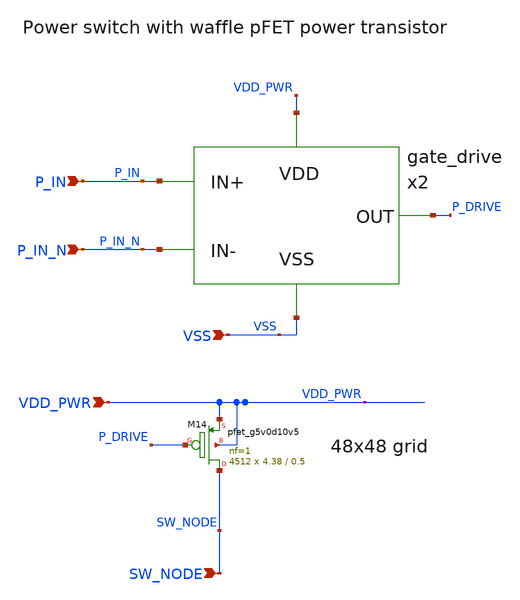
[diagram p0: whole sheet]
** sch_path: xschem/power_stage.sch
**.subckt power_stage P_IN P_IN_N SW_NODE VDD_PWR VSS
*.ipin P_IN
*.ipin P_IN_N
*.ipin SW_NODE
*.ipin VDD_PWR
*.ipin VSS
XM14 SW_NODE P_DRIVE VDD_PWR VDD_PWR sky130_fd_pr__pfet_g5v0d10v5 L=0.5 W=4.38 nf=1 ad='int((nf+1)/2) * W/nf * 0.29'
+ as='int((nf+2)/2) * W/nf * 0.29' pd='2*int((nf+1)/2) * (W/nf + 0.29)' ps='2*int((nf+2)/2) * (W/nf + 0.29)'
+ nrd='0.29 / W' nrs='0.29 / W' sa=0 sb=0 sd=0 mult=4512 m=4512
x2 P_IN P_IN_N VDD_PWR VSS P_DRIVE gate_drive
**.ends

* expanding   symbol:  gate_drive.sym # of pins=5
** sym_path: gate_drive.sym
** sch_path: gate_drive.sch
.subckt gate_drive IN_P IN_M VDD VSS OUT
*.ipin IN_M
*.ipin IN_P
*.ipin VDD
*.ipin VSS
*.opin OUT
XM1 net1 IN_P VSS VSS sky130_fd_pr__nfet_g5v0d10v5 L=0.5 W=2 nf=1 ad='int((nf+1)/2) * W/nf * 0.29' as='int((nf+2)/2) * W/nf * 0.29'
+ pd='2*int((nf+1)/2) * (W/nf + 0.29)' ps='2*int((nf+2)/2) * (W/nf + 0.29)' nrd='0.29 / W' nrs='0.29 / W'
+ sa=0 sb=0 sd=0 mult=2 m=2
XM2 net1 S1_N VDD VDD sky130_fd_pr__pfet_g5v0d10v5 L=0.5 W=4 nf=1 ad='int((nf+1)/2) * W/nf * 0.29' as='int((nf+2)/2) * W/nf * 0.29'
+ pd='2*int((nf+1)/2) * (W/nf + 0.29)' ps='2*int((nf+2)/2) * (W/nf + 0.29)' nrd='0.29 / W' nrs='0.29 / W'
+ sa=0 sb=0 sd=0 mult=2 m=2
XM3 S1_N IN_M VSS VSS sky130_fd_pr__nfet_g5v0d10v5 L=0.5 W=2 nf=1 ad='int((nf+1)/2) * W/nf * 0.29' as='int((nf+2)/2) * W/nf * 0.29'
+ pd='2*int((nf+1)/2) * (W/nf + 0.29)' ps='2*int((nf+2)/2) * (W/nf + 0.29)' nrd='0.29 / W' nrs='0.29 / W'
+ sa=0 sb=0 sd=0 mult=2 m=2
XM4 S1_N net1 VDD VDD sky130_fd_pr__pfet_g5v0d10v5 L=0.5 W=4 nf=1 ad='int((nf+1)/2) * W/nf * 0.29' as='int((nf+2)/2) * W/nf * 0.29'
+ pd='2*int((nf+1)/2) * (W/nf + 0.29)' ps='2*int((nf+2)/2) * (W/nf + 0.29)' nrd='0.29 / W' nrs='0.29 / W'
+ sa=0 sb=0 sd=0 mult=2 m=2
XM5 S2_N S1_N VDD VDD sky130_fd_pr__pfet_g5v0d10v5 L=0.5 W=15 nf=1 ad='int((nf+1)/2) * W/nf * 0.29' as='int((nf+2)/2) * W/nf * 0.29'
+ pd='2*int((nf+1)/2) * (W/nf + 0.29)' ps='2*int((nf+2)/2) * (W/nf + 0.29)' nrd='0.29 / W' nrs='0.29 / W'
+ sa=0 sb=0 sd=0 mult=2 m=2
XM6 S2_N S1_N VSS VSS sky130_fd_pr__nfet_g5v0d10v5 L=0.5 W=7 nf=1 ad='int((nf+1)/2) * W/nf * 0.29' as='int((nf+2)/2) * W/nf * 0.29'
+ pd='2*int((nf+1)/2) * (W/nf + 0.29)' ps='2*int((nf+2)/2) * (W/nf + 0.29)' nrd='0.29 / W' nrs='0.29 / W'
+ sa=0 sb=0 sd=0 mult=2 m=2
XM7 S3_N S2_N VDD VDD sky130_fd_pr__pfet_g5v0d10v5 L=0.5 W=15 nf=1 ad='int((nf+1)/2) * W/nf * 0.29' as='int((nf+2)/2) * W/nf * 0.29'
+ pd='2*int((nf+1)/2) * (W/nf + 0.29)' ps='2*int((nf+2)/2) * (W/nf + 0.29)' nrd='0.29 / W' nrs='0.29 / W'
+ sa=0 sb=0 sd=0 mult=6 m=6
XM8 S3_N S2_N VSS VSS sky130_fd_pr__nfet_g5v0d10v5 L=0.5 W=7 nf=1 ad='int((nf+1)/2) * W/nf * 0.29' as='int((nf+2)/2) * W/nf * 0.29'
+ pd='2*int((nf+1)/2) * (W/nf + 0.29)' ps='2*int((nf+2)/2) * (W/nf + 0.29)' nrd='0.29 / W' nrs='0.29 / W'
+ sa=0 sb=0 sd=0 mult=6 m=6
XM9 S4_N S3_N VDD VDD sky130_fd_pr__pfet_g5v0d10v5 L=0.5 W=15 nf=1 ad='int((nf+1)/2) * W/nf * 0.29' as='int((nf+2)/2) * W/nf * 0.29'
+ pd='2*int((nf+1)/2) * (W/nf + 0.29)' ps='2*int((nf+2)/2) * (W/nf + 0.29)' nrd='0.29 / W' nrs='0.29 / W'
+ sa=0 sb=0 sd=0 mult=20 m=20
XM10 S4_N S3_N VSS VSS sky130_fd_pr__nfet_g5v0d10v5 L=0.5 W=7 nf=1 ad='int((nf+1)/2) * W/nf * 0.29' as='int((nf+2)/2) * W/nf * 0.29'
+ pd='2*int((nf+1)/2) * (W/nf + 0.29)' ps='2*int((nf+2)/2) * (W/nf + 0.29)' nrd='0.29 / W' nrs='0.29 / W'
+ sa=0 sb=0 sd=0 mult=20 m=20
XM11 OUT S4_N VDD VDD sky130_fd_pr__pfet_g5v0d10v5 L=0.5 W=15 nf=1 ad='int((nf+1)/2) * W/nf * 0.29' as='int((nf+2)/2) * W/nf * 0.29'
+ pd='2*int((nf+1)/2) * (W/nf + 0.29)' ps='2*int((nf+2)/2) * (W/nf + 0.29)' nrd='0.29 / W' nrs='0.29 / W'
+ sa=0 sb=0 sd=0 mult=60 m=60
XM12 OUT S4_N VSS VSS sky130_fd_pr__nfet_g5v0d10v5 L=0.5 W=7 nf=1 ad='int((nf+1)/2) * W/nf * 0.29' as='int((nf+2)/2) * W/nf * 0.29'
+ pd='2*int((nf+1)/2) * (W/nf + 0.29)' ps='2*int((nf+2)/2) * (W/nf + 0.29)' nrd='0.29 / W' nrs='0.29 / W'
+ sa=0 sb=0 sd=0 mult=60 m=60
.ends

.end
